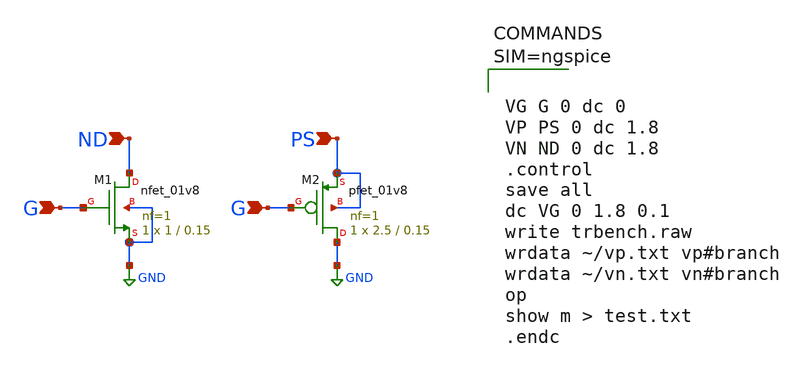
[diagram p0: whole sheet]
** sch_path: trbench.sch
**.subckt trbench ND G G PS
*.ipin ND
*.ipin G
*.ipin G
*.ipin PS
XM2 GND G PS PS sky130_fd_pr__pfet_01v8 L=0.15 W=2.5 nf=1 ad='int((nf+1)/2) * W/nf * 0.29' as='int((nf+2)/2) * W/nf * 0.29'
+ pd='2*int((nf+1)/2) * (W/nf + 0.29)' ps='2*int((nf+2)/2) * (W/nf + 0.29)' nrd='0.29 / W' nrs='0.29 / W'
+ sa=0 sb=0 sd=0 mult=1 m=1
XM1 ND G GND GND sky130_fd_pr__nfet_01v8 L=0.15 W=1 nf=1 ad='int((nf+1)/2) * W/nf * 0.29' as='int((nf+2)/2) * W/nf * 0.29'
+ pd='2*int((nf+1)/2) * (W/nf + 0.29)' ps='2*int((nf+2)/2) * (W/nf + 0.29)' nrd='0.29 / W' nrs='0.29 / W'
+ sa=0 sb=0 sd=0 mult=1 m=1
**** begin user architecture code

** opencircuitdesign pdks install
.lib $::SKYWATER_MODELS/sky130.lib.spice tt





VG G 0 dc 0
VP PS 0 dc 1.8
VN ND 0 dc 1.8
.control
save all
dc VG 0 1.8 0.1
write trbench.raw
wrdata ~/vp.txt vp#branch
wrdata ~/vn.txt vn#branch
op
show m > test.txt
.endc



**** end user architecture code
**.ends
.GLOBAL GND
.end
